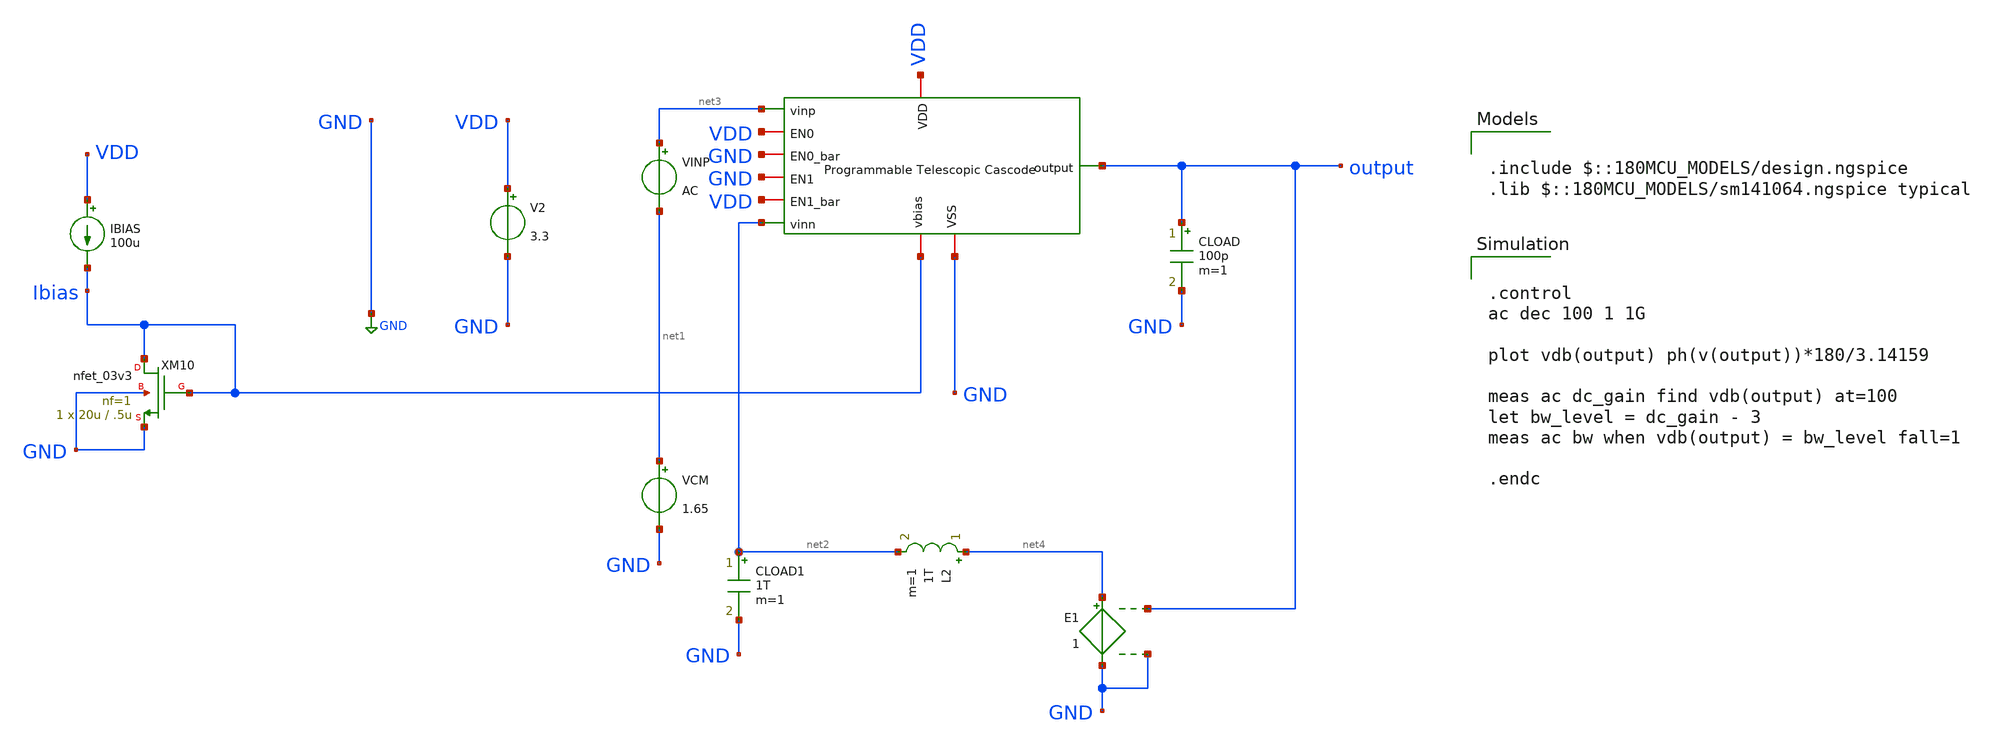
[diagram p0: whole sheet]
** sch_path: designs/libs/tb_amps/tb_ota_telescopic/programmable_telescopic_cascode_ac_open_tb.sch
**.subckt programmable_telescopic_cascode_ac_open_tb
IBIAS VDD Ibias 100u
V2 VDD GND 3.3
CLOAD output GND 100p m=1
VINP net3 net1 AC
VCM net1 GND 1.65
L2 net4 net2 1T m=1
CLOAD1 net2 GND 1T m=1
E1 net4 GND output GND 1
XM10 Ibias Ibias GND GND nfet_03v3 L=.5u W=20u nf=1 ad='int((nf+1)/2) * W/nf * 0.18u' as='int((nf+2)/2) * W/nf * 0.18u'
+ pd='2*int((nf+1)/2) * (W/nf + 0.18u)' ps='2*int((nf+2)/2) * (W/nf + 0.18u)' nrd='0.18u / W' nrs='0.18u / W'
+ sa=0 sb=0 sd=0 m=1
x1 VDD output VDD GND GND VDD net2 net3 GND Ibias programmable_telescopic_cascode
**** begin user architecture code

.include $::180MCU_MODELS/design.ngspice
.lib $::180MCU_MODELS/sm141064.ngspice typical



.control
ac dec 100 1 1G

plot vdb(output) ph(v(output))*180/3.14159

meas ac dc_gain find vdb(output) at=100
let bw_level = dc_gain - 3
meas ac bw when vdb(output) = bw_level fall=1

.endc



**** end user architecture code
**.ends
.GLOBAL GND
.end
